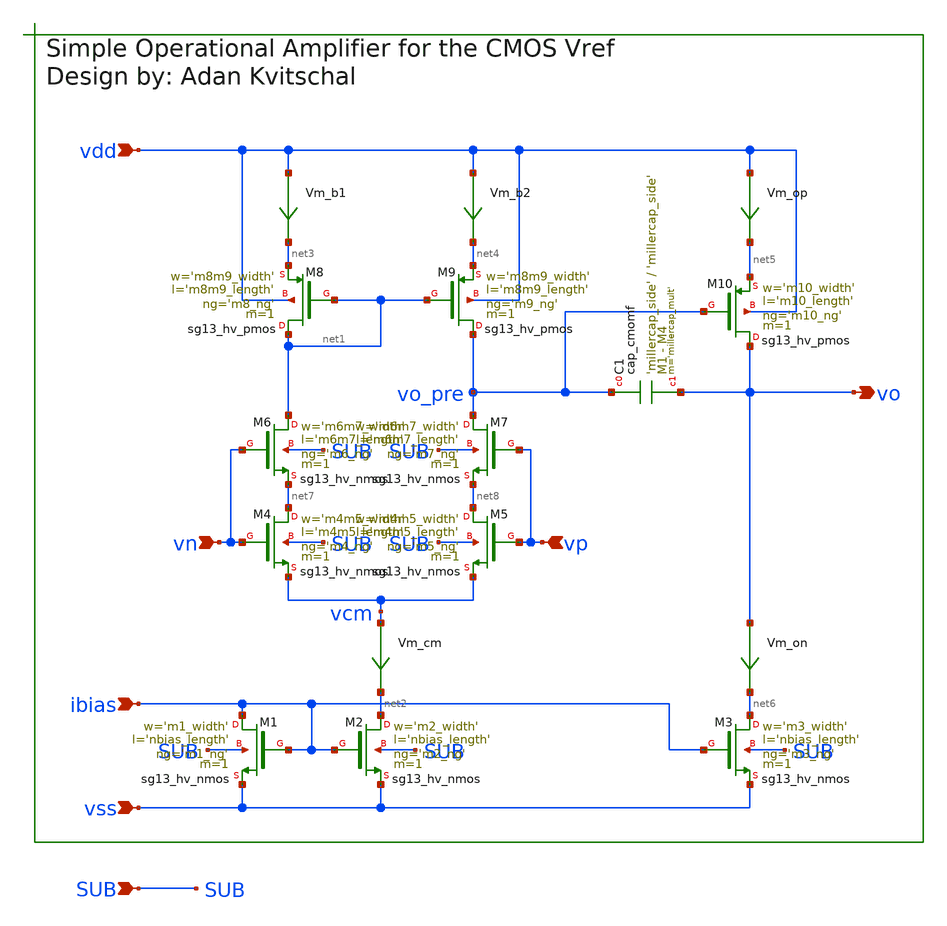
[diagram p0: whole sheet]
** sch_path: sch/output_amp/output_amp_def.sch
**.subckt output_amp_def vp vn ibias vo vss vdd SUB
*.ipin vp
*.ipin vn
*.ipin ibias
*.opin vo
*.ipin vss
*.ipin vdd
*.ipin SUB
Vm_b1 vdd net3 0
.save i(vm_b1)
Vm_op vdd net5 0
.save i(vm_op)
Vm_cm vcm net2 0
.save i(vm_cm)
Vm_b2 vdd net4 0
.save i(vm_b2)
Vm_on vo net6 0
.save i(vm_on)
XM1 ibias ibias vss SUB sg13_hv_nmos w='m1_width' l='nbias_length' ng='m1_ng' m=1 mm_ok=1
XM2 net2 ibias vss SUB sg13_hv_nmos w='m2_width' l='nbias_length' ng='m2_ng' m=1 mm_ok=1
XM3 net6 ibias vss SUB sg13_hv_nmos w='m3_width' l='nbias_length' ng='m3_ng' m=1 mm_ok=1
XM4 net7 vn vcm SUB sg13_hv_nmos w='m4m5_width' l='m4m5_length' ng='m4_ng' m=1 mm_ok=1
XM5 net8 vp vcm SUB sg13_hv_nmos w='m4m5_width' l='m4m5_length' ng='m5_ng' m=1 mm_ok=1
XM6 net1 vn net7 SUB sg13_hv_nmos w='m6m7_width' l='m6m7_length' ng='m6_ng' m=1 mm_ok=1
XM7 vo_pre vp net8 SUB sg13_hv_nmos w='m6m7_width' l='m6m7_length' ng='m7_ng' m=1 mm_ok=1
XM8 net1 net1 net3 vdd sg13_hv_pmos w='m8m9_width' l='m8m9_length' ng='m8_ng' m=1 mm_ok=1
XM9 vo_pre net1 net4 vdd sg13_hv_pmos w='m8m9_width' l='m8m9_length' ng='m9_ng' m=1 mm_ok=1
XM10 vo vo_pre net5 vdd sg13_hv_pmos w='m10_width' l='m10_length' ng='m10_ng' m=1 mm_ok=1
XC1 vo_pre vo cap_cmomf w='millercap_side' l='millercap_side' mmin=1 mmax=4 subblock=0 rfmodel=0 subscale=1
+ m='millercap_mult' mm_ok=1
**.ends
.end
